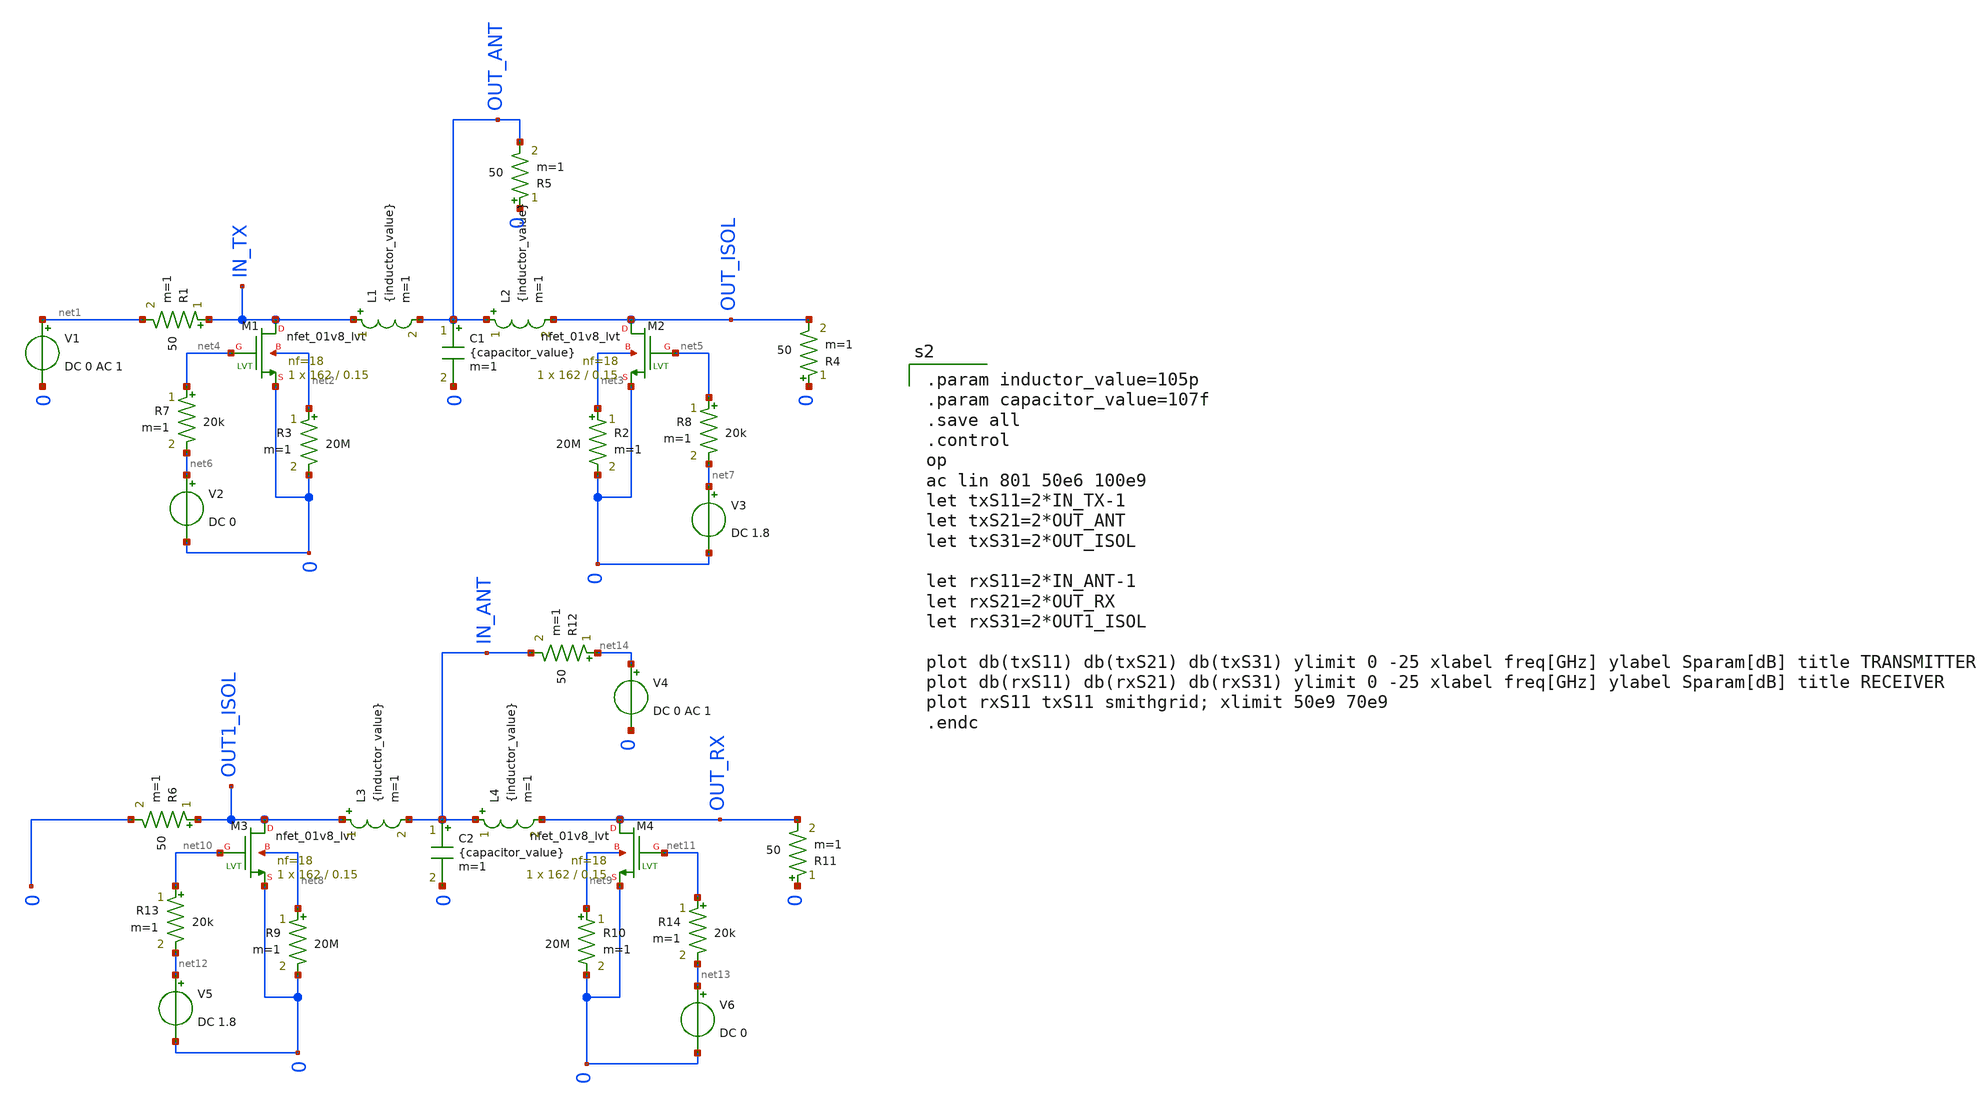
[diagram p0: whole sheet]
** sch_path: Switch_tapeout/xschem/testSwitchCircuit.sch
**.subckt testSwitchCircuit
R1 IN_TX net1 50 m=1
XM1 IN_TX net4 0 net2 sky130_fd_pr__nfet_01v8_lvt L=0.15 W=162 nf=18 ad='int((nf+1)/2) * W/nf * 0.29'
+ as='int((nf+2)/2) * W/nf * 0.29' pd='2*int((nf+1)/2) * (W/nf + 0.29)' ps='2*int((nf+2)/2) * (W/nf + 0.29)'
+ nrd='0.29 / W' nrs='0.29 / W' sa=0 sb=0 sd=0 mult=1 m=1
R3 net2 0 20M m=1
V1 net1 0 DC 0 AC 1
XM2 OUT_ISOL net5 0 net3 sky130_fd_pr__nfet_01v8_lvt L=0.15 W=162 nf=18 ad='int((nf+1)/2) * W/nf * 0.29'
+ as='int((nf+2)/2) * W/nf * 0.29' pd='2*int((nf+1)/2) * (W/nf + 0.29)' ps='2*int((nf+2)/2) * (W/nf + 0.29)'
+ nrd='0.29 / W' nrs='0.29 / W' sa=0 sb=0 sd=0 mult=1 m=1
R2 net3 0 20M m=1
L1 IN_TX OUT_ANT {inductor_value} m=1
L2 OUT_ANT OUT_ISOL {inductor_value} m=1
V2 net6 0 DC 0
V3 net7 0 DC 1.8
R4 0 OUT_ISOL 50 m=1
R5 0 OUT_ANT 50 m=1
R7 net4 net6 20k m=1
R8 net5 net7 20k m=1
C1 OUT_ANT 0 {capacitor_value} m=1
R6 OUT1_ISOL 0 50 m=1
XM3 OUT1_ISOL net10 0 net8 sky130_fd_pr__nfet_01v8_lvt L=0.15 W=162 nf=18 ad='int((nf+1)/2) * W/nf * 0.29'
+ as='int((nf+2)/2) * W/nf * 0.29' pd='2*int((nf+1)/2) * (W/nf + 0.29)' ps='2*int((nf+2)/2) * (W/nf + 0.29)'
+ nrd='0.29 / W' nrs='0.29 / W' sa=0 sb=0 sd=0 mult=1 m=1
R9 net8 0 20M m=1
V4 net14 0 DC 0 AC 1
XM4 OUT_RX net11 0 net9 sky130_fd_pr__nfet_01v8_lvt L=0.15 W=162 nf=18 ad='int((nf+1)/2) * W/nf * 0.29'
+ as='int((nf+2)/2) * W/nf * 0.29' pd='2*int((nf+1)/2) * (W/nf + 0.29)' ps='2*int((nf+2)/2) * (W/nf + 0.29)'
+ nrd='0.29 / W' nrs='0.29 / W' sa=0 sb=0 sd=0 mult=1 m=1
R10 net9 0 20M m=1
L3 OUT1_ISOL IN_ANT {inductor_value} m=1
L4 IN_ANT OUT_RX {inductor_value} m=1
V5 net12 0 DC 1.8
V6 net13 0 DC 0
R11 0 OUT_RX 50 m=1
R12 net14 IN_ANT 50 m=1
R13 net10 net12 20k m=1
R14 net11 net13 20k m=1
C2 IN_ANT 0 {capacitor_value} m=1
**** begin user architecture code

.option wnflag = 1
.lib /home/leonardo/skywater-pdk/libraries/sky130_fd_pr/latest/models/sky130.lib.spice tt
.MODEL Ustrip_50ohm TRLA (R=0.00762 L=3.082e-13 G=3.187e-6 C=1.289e-16 Len=500)
* Corner
*.include $::SKYWATER_MODELS/models/corners/tt/rf.spice


.param inductor_value=105p
.param capacitor_value=107f
.save all
.control
op
ac lin 801 50e6 100e9
let txS11=2*IN_TX-1
let txS21=2*OUT_ANT
let txS31=2*OUT_ISOL

let rxS11=2*IN_ANT-1
let rxS21=2*OUT_RX
let rxS31=2*OUT1_ISOL

plot db(txS11) db(txS21) db(txS31) ylimit 0 -25 xlabel freq[GHz] ylabel Sparam[dB] title TRANSMITTER
plot db(rxS11) db(rxS21) db(rxS31) ylimit 0 -25 xlabel freq[GHz] ylabel Sparam[dB] title RECEIVER
plot rxS11 txS11 smithgrid; xlimit 50e9 70e9
.endc


**** end user architecture code
**.ends
.end
